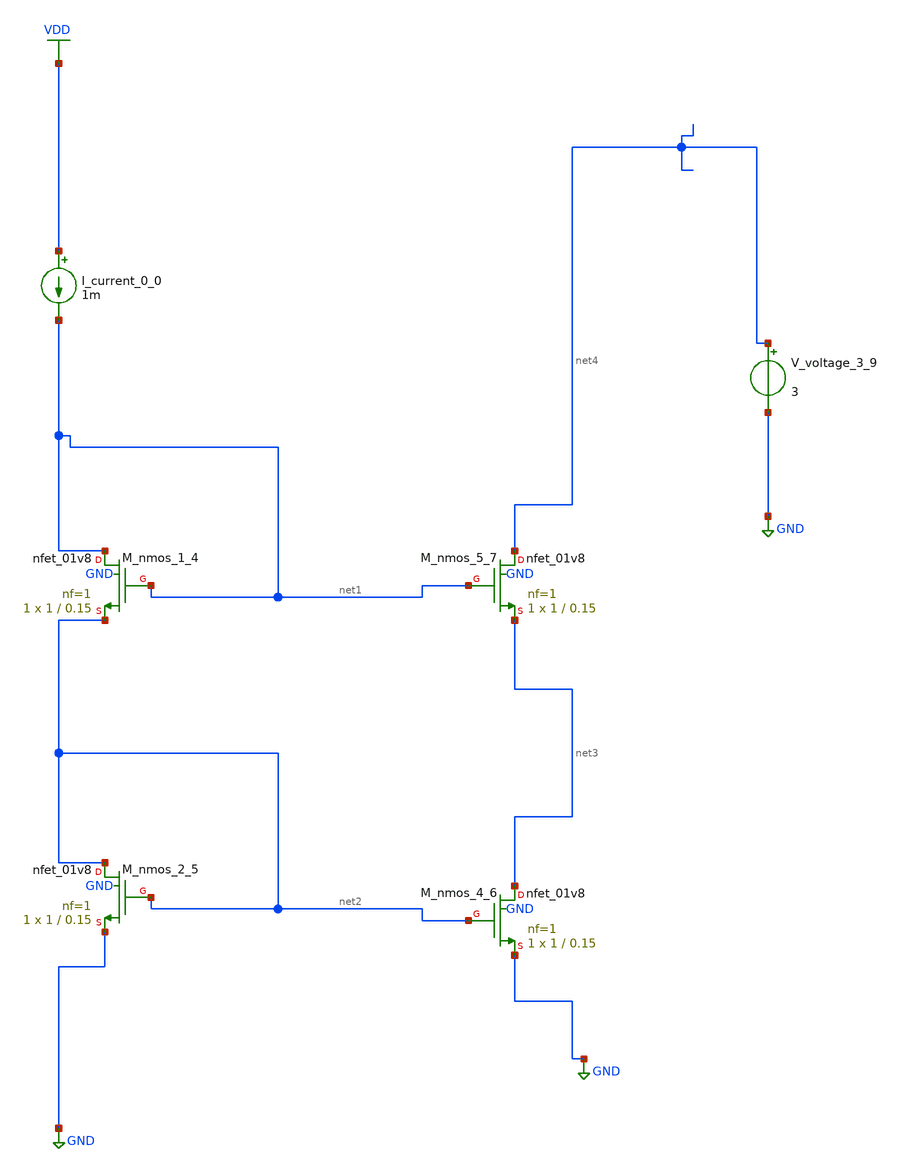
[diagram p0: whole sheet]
** sch_path: schematics/AMSNet/260.sch
**.subckt 260
I_current_0_0 VDD net1 1m
XM_nmos_1_4 net1 net1 net2 GND sky130_fd_pr__nfet_01v8 L=0.15 W=1 nf=1 ad='int((1 + 1)/2) * 1 / 1 * 0.29'
+ as='int((1 + 2)/2) * 1 / 1 * 0.29' pd='2*int((1 + 1)/2) * (1 / 1 + 0.29)' ps='2*int((1 + 2)/2) * (1 / 1 + 0.29)'
+ nrd='0.29 / 1 ' nrs='0.29 / 1 ' sa=0 sb=0 sd=0 mult=1 m=1
XM_nmos_2_5 net2 net2 GND GND sky130_fd_pr__nfet_01v8 L=0.15 W=1 nf=1 ad='int((1 + 1)/2) * 1 / 1 * 0.29'
+ as='int((1 + 2)/2) * 1 / 1 * 0.29' pd='2*int((1 + 1)/2) * (1 / 1 + 0.29)' ps='2*int((1 + 2)/2) * (1 / 1 + 0.29)'
+ nrd='0.29 / 1 ' nrs='0.29 / 1 ' sa=0 sb=0 sd=0 mult=1 m=1
XM_nmos_4_6 net3 net2 GND GND sky130_fd_pr__nfet_01v8 L=0.15 W=1 nf=1 ad='int((1 + 1)/2) * 1 / 1 * 0.29'
+ as='int((1 + 2)/2) * 1 / 1 * 0.29' pd='2*int((1 + 1)/2) * (1 / 1 + 0.29)' ps='2*int((1 + 2)/2) * (1 / 1 + 0.29)'
+ nrd='0.29 / 1 ' nrs='0.29 / 1 ' sa=0 sb=0 sd=0 mult=1 m=1
XM_nmos_5_7 net4 net1 net3 GND sky130_fd_pr__nfet_01v8 L=0.15 W=1 nf=1 ad='int((1 + 1)/2) * 1 / 1 * 0.29'
+ as='int((1 + 2)/2) * 1 / 1 * 0.29' pd='2*int((1 + 1)/2) * (1 / 1 + 0.29)' ps='2*int((1 + 2)/2) * (1 / 1 + 0.29)'
+ nrd='0.29 / 1 ' nrs='0.29 / 1 ' sa=0 sb=0 sd=0 mult=1 m=1
V_voltage_3_9 net4 GND 3
**.ends
.GLOBAL GND
.GLOBAL VDD
.end
